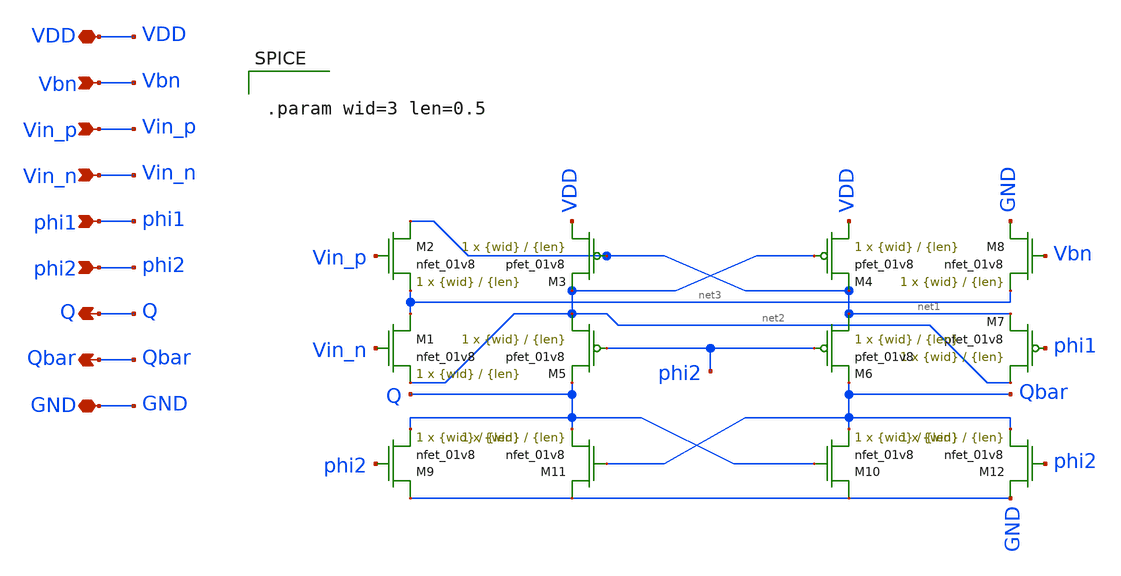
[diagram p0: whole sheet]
** sch_path: final/LDS/comparator_LDS.sch
**.subckt comparator_LDS Vin_p Vin_n Vbn phi1 phi2 Q Qbar VDD GND
*.ipin Vin_p
*.ipin Vin_n
*.ipin Vbn
*.ipin phi1
*.ipin phi2
*.opin Q
*.opin Qbar
*.iopin VDD
*.iopin GND
XM2 net1 Vin_p net3 GND sky130_fd_pr__nfet_01v8 L={len} W={wid} nf=1 ad='int((nf+1)/2) * W/nf * 0.29'
+ as='int((nf+2)/2) * W/nf * 0.29' pd='2*int((nf+1)/2) * (W/nf + 0.29)' ps='2*int((nf+2)/2) * (W/nf + 0.29)'
+ nrd='0.29 / W' nrs='0.29 / W' sa=0 sb=0 sd=0 mult=1 m=1
XM3 VDD net1 net2 VDD sky130_fd_pr__pfet_01v8 L={len} W={wid} nf=1 ad='int((nf+1)/2) * W/nf * 0.29' as='int((nf+2)/2) * W/nf * 0.29'
+ pd='2*int((nf+1)/2) * (W/nf + 0.29)' ps='2*int((nf+2)/2) * (W/nf + 0.29)' nrd='0.29 / W' nrs='0.29 / W'
+ sa=0 sb=0 sd=0 mult=1 m=1
XM4 VDD net2 net1 VDD sky130_fd_pr__pfet_01v8 L={len} W={wid} nf=1 ad='int((nf+1)/2) * W/nf * 0.29' as='int((nf+2)/2) * W/nf * 0.29'
+ pd='2*int((nf+1)/2) * (W/nf + 0.29)' ps='2*int((nf+2)/2) * (W/nf + 0.29)' nrd='0.29 / W' nrs='0.29 / W'
+ sa=0 sb=0 sd=0 mult=1 m=1
XM7 net2 phi1 net1 VDD sky130_fd_pr__pfet_01v8 L={len} W={wid} nf=1 ad='int((nf+1)/2) * W/nf * 0.29'
+ as='int((nf+2)/2) * W/nf * 0.29' pd='2*int((nf+1)/2) * (W/nf + 0.29)' ps='2*int((nf+2)/2) * (W/nf + 0.29)'
+ nrd='0.29 / W' nrs='0.29 / W' sa=0 sb=0 sd=0 mult=1 m=1
XM5 net2 phi2 Q VDD sky130_fd_pr__pfet_01v8 L={len} W={wid} nf=1 ad='int((nf+1)/2) * W/nf * 0.29' as='int((nf+2)/2) * W/nf * 0.29'
+ pd='2*int((nf+1)/2) * (W/nf + 0.29)' ps='2*int((nf+2)/2) * (W/nf + 0.29)' nrd='0.29 / W' nrs='0.29 / W'
+ sa=0 sb=0 sd=0 mult=1 m=1
XM6 net1 phi2 Qbar VDD sky130_fd_pr__pfet_01v8 L={len} W={wid} nf=1 ad='int((nf+1)/2) * W/nf * 0.29'
+ as='int((nf+2)/2) * W/nf * 0.29' pd='2*int((nf+1)/2) * (W/nf + 0.29)' ps='2*int((nf+2)/2) * (W/nf + 0.29)'
+ nrd='0.29 / W' nrs='0.29 / W' sa=0 sb=0 sd=0 mult=1 m=1
XM1 net3 Vin_n net2 GND sky130_fd_pr__nfet_01v8 L={len} W={wid} nf=1 ad='int((nf+1)/2) * W/nf * 0.29'
+ as='int((nf+2)/2) * W/nf * 0.29' pd='2*int((nf+1)/2) * (W/nf + 0.29)' ps='2*int((nf+2)/2) * (W/nf + 0.29)'
+ nrd='0.29 / W' nrs='0.29 / W' sa=0 sb=0 sd=0 mult=1 m=1
XM8 GND Vbn net3 GND sky130_fd_pr__nfet_01v8 L={len} W={wid} nf=1 ad='int((nf+1)/2) * W/nf * 0.29' as='int((nf+2)/2) * W/nf * 0.29'
+ pd='2*int((nf+1)/2) * (W/nf + 0.29)' ps='2*int((nf+2)/2) * (W/nf + 0.29)' nrd='0.29 / W' nrs='0.29 / W'
+ sa=0 sb=0 sd=0 mult=1 m=1
XM9 GND phi2 Q GND sky130_fd_pr__nfet_01v8 L={len} W={wid} nf=1 ad='int((nf+1)/2) * W/nf * 0.29' as='int((nf+2)/2) * W/nf * 0.29'
+ pd='2*int((nf+1)/2) * (W/nf + 0.29)' ps='2*int((nf+2)/2) * (W/nf + 0.29)' nrd='0.29 / W' nrs='0.29 / W'
+ sa=0 sb=0 sd=0 mult=1 m=1
XM10 GND Q Qbar GND sky130_fd_pr__nfet_01v8 L={len} W={wid} nf=1 ad='int((nf+1)/2) * W/nf * 0.29' as='int((nf+2)/2) * W/nf * 0.29'
+ pd='2*int((nf+1)/2) * (W/nf + 0.29)' ps='2*int((nf+2)/2) * (W/nf + 0.29)' nrd='0.29 / W' nrs='0.29 / W'
+ sa=0 sb=0 sd=0 mult=1 m=1
XM11 GND Qbar Q GND sky130_fd_pr__nfet_01v8 L={len} W={wid} nf=1 ad='int((nf+1)/2) * W/nf * 0.29' as='int((nf+2)/2) * W/nf * 0.29'
+ pd='2*int((nf+1)/2) * (W/nf + 0.29)' ps='2*int((nf+2)/2) * (W/nf + 0.29)' nrd='0.29 / W' nrs='0.29 / W'
+ sa=0 sb=0 sd=0 mult=1 m=1
XM12 GND phi2 Qbar GND sky130_fd_pr__nfet_01v8 L={len} W={wid} nf=1 ad='int((nf+1)/2) * W/nf * 0.29'
+ as='int((nf+2)/2) * W/nf * 0.29' pd='2*int((nf+1)/2) * (W/nf + 0.29)' ps='2*int((nf+2)/2) * (W/nf + 0.29)'
+ nrd='0.29 / W' nrs='0.29 / W' sa=0 sb=0 sd=0 mult=1 m=1
**** begin user architecture code


.param wid=3 len=0.5


**** end user architecture code
**.ends
.end
